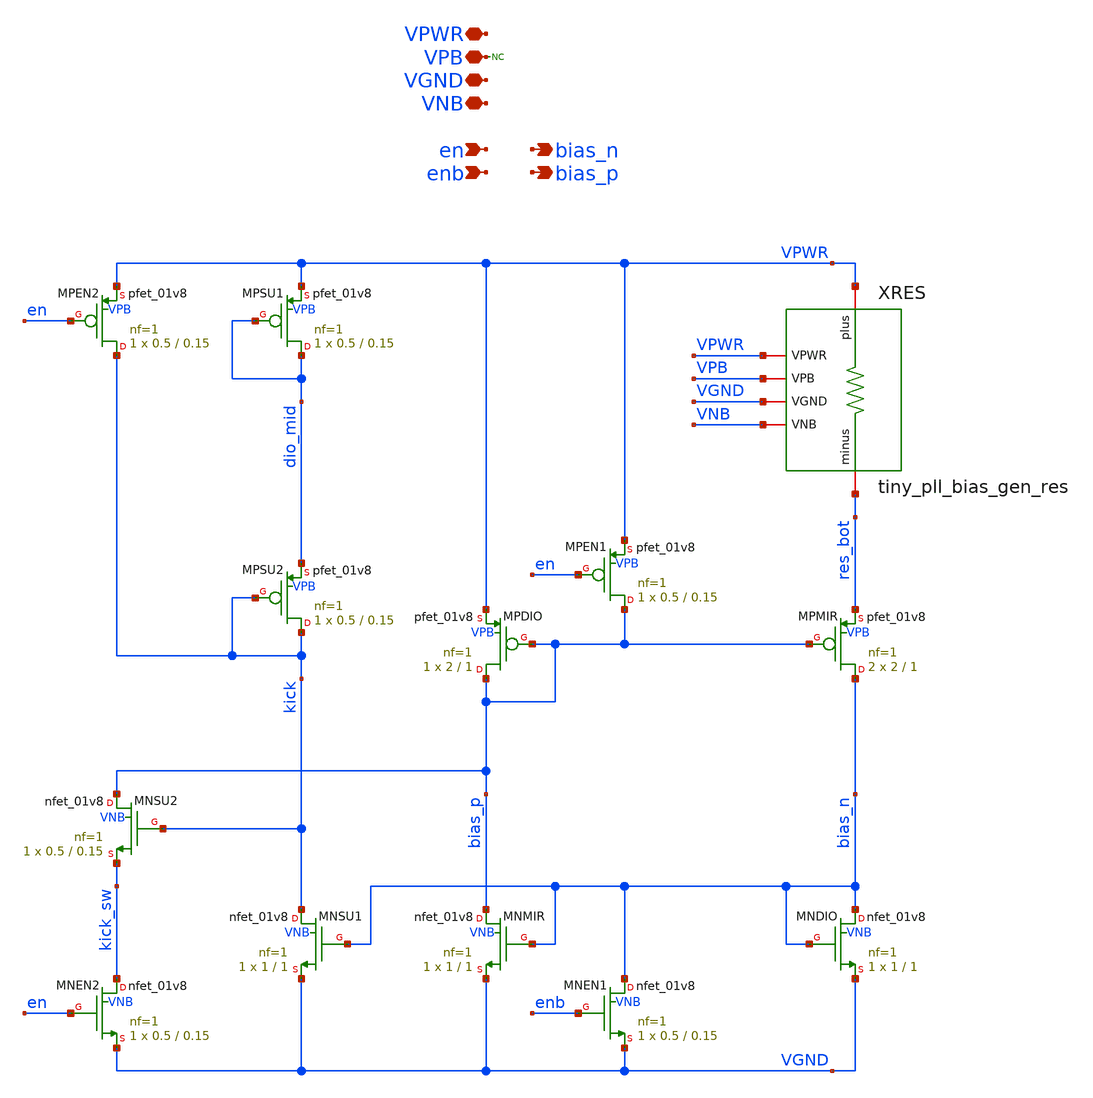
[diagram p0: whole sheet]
** sch_path: xschem/tiny_pll/tiny_pll_bias_gen.sch
**.subckt tiny_pll_bias_gen VNB VGND VPB VPWR bias_n enb en bias_p
*.iopin VNB
*.iopin VGND
*.iopin VPB
*.iopin VPWR
*.opin bias_n
*.ipin enb
*.ipin en
*.opin bias_p
XMNMIR bias_p bias_n VGND VNB sky130_fd_pr__nfet_01v8 L=1 W=1 nf=1 ad='int((nf+1)/2) * W/nf * 0.29' as='int((nf+2)/2) * W/nf * 0.29'
+ pd='2*int((nf+1)/2) * (W/nf + 0.29)' ps='2*int((nf+2)/2) * (W/nf + 0.29)' nrd='0.29 / W' nrs='0.29 / W'
+ sa=0 sb=0 sd=0 mult=1 m=1
XMNDIO bias_n bias_n VGND VNB sky130_fd_pr__nfet_01v8 L=1 W=1 nf=1 ad='int((nf+1)/2) * W/nf * 0.29' as='int((nf+2)/2) * W/nf * 0.29'
+ pd='2*int((nf+1)/2) * (W/nf + 0.29)' ps='2*int((nf+2)/2) * (W/nf + 0.29)' nrd='0.29 / W' nrs='0.29 / W'
+ sa=0 sb=0 sd=0 mult=1 m=1
XMPDIO bias_p bias_p VPWR VPB sky130_fd_pr__pfet_01v8 L=1 W=2 nf=1 ad='int((nf+1)/2) * W/nf * 0.29' as='int((nf+2)/2) * W/nf * 0.29'
+ pd='2*int((nf+1)/2) * (W/nf + 0.29)' ps='2*int((nf+2)/2) * (W/nf + 0.29)' nrd='0.29 / W' nrs='0.29 / W'
+ sa=0 sb=0 sd=0 mult=1 m=1
XMPMIR bias_n bias_p res_bot VPB sky130_fd_pr__pfet_01v8 L=1 W=2 nf=1 ad='int((nf+1)/2) * W/nf * 0.29'
+ as='int((nf+2)/2) * W/nf * 0.29' pd='2*int((nf+1)/2) * (W/nf + 0.29)' ps='2*int((nf+2)/2) * (W/nf + 0.29)'
+ nrd='0.29 / W' nrs='0.29 / W' sa=0 sb=0 sd=0 mult=2 m=2
* noconn VPB
XMNEN1 bias_n enb VGND VNB sky130_fd_pr__nfet_01v8 L=0.15 W=0.5 nf=1 ad='int((nf+1)/2) * W/nf * 0.29'
+ as='int((nf+2)/2) * W/nf * 0.29' pd='2*int((nf+1)/2) * (W/nf + 0.29)' ps='2*int((nf+2)/2) * (W/nf + 0.29)'
+ nrd='0.29 / W' nrs='0.29 / W' sa=0 sb=0 sd=0 mult=1 m=1
XMPEN1 bias_p en VPWR VPB sky130_fd_pr__pfet_01v8 L=0.15 W=0.5 nf=1 ad='int((nf+1)/2) * W/nf * 0.29'
+ as='int((nf+2)/2) * W/nf * 0.29' pd='2*int((nf+1)/2) * (W/nf + 0.29)' ps='2*int((nf+2)/2) * (W/nf + 0.29)'
+ nrd='0.29 / W' nrs='0.29 / W' sa=0 sb=0 sd=0 mult=1 m=1
XRES VGND VNB VPWR VPB VPWR res_bot tiny_pll_bias_gen_res
XMNSU1 kick bias_n VGND VNB sky130_fd_pr__nfet_01v8 L=1 W=1 nf=1 ad='int((nf+1)/2) * W/nf * 0.29' as='int((nf+2)/2) * W/nf * 0.29'
+ pd='2*int((nf+1)/2) * (W/nf + 0.29)' ps='2*int((nf+2)/2) * (W/nf + 0.29)' nrd='0.29 / W' nrs='0.29 / W'
+ sa=0 sb=0 sd=0 mult=1 m=1
XMNSU2 bias_p kick kick_sw VNB sky130_fd_pr__nfet_01v8 L=0.15 W=0.5 nf=1 ad='int((nf+1)/2) * W/nf * 0.29'
+ as='int((nf+2)/2) * W/nf * 0.29' pd='2*int((nf+1)/2) * (W/nf + 0.29)' ps='2*int((nf+2)/2) * (W/nf + 0.29)'
+ nrd='0.29 / W' nrs='0.29 / W' sa=0 sb=0 sd=0 mult=1 m=1
XMNEN2 kick_sw en VGND VNB sky130_fd_pr__nfet_01v8 L=0.15 W=0.5 nf=1 ad='int((nf+1)/2) * W/nf * 0.29'
+ as='int((nf+2)/2) * W/nf * 0.29' pd='2*int((nf+1)/2) * (W/nf + 0.29)' ps='2*int((nf+2)/2) * (W/nf + 0.29)'
+ nrd='0.29 / W' nrs='0.29 / W' sa=0 sb=0 sd=0 mult=1 m=1
XMPEN2 kick en VPWR VPB sky130_fd_pr__pfet_01v8 L=0.15 W=0.5 nf=1 ad='int((nf+1)/2) * W/nf * 0.29' as='int((nf+2)/2) * W/nf * 0.29'
+ pd='2*int((nf+1)/2) * (W/nf + 0.29)' ps='2*int((nf+2)/2) * (W/nf + 0.29)' nrd='0.29 / W' nrs='0.29 / W'
+ sa=0 sb=0 sd=0 mult=1 m=1
XMPSU2 kick kick dio_mid VPB sky130_fd_pr__pfet_01v8 L=0.15 W=0.5 nf=1 ad='int((nf+1)/2) * W/nf * 0.29'
+ as='int((nf+2)/2) * W/nf * 0.29' pd='2*int((nf+1)/2) * (W/nf + 0.29)' ps='2*int((nf+2)/2) * (W/nf + 0.29)'
+ nrd='0.29 / W' nrs='0.29 / W' sa=0 sb=0 sd=0 mult=1 m=1
XMPSU1 dio_mid dio_mid VPWR VPB sky130_fd_pr__pfet_01v8 L=0.15 W=0.5 nf=1 ad='int((nf+1)/2) * W/nf * 0.29'
+ as='int((nf+2)/2) * W/nf * 0.29' pd='2*int((nf+1)/2) * (W/nf + 0.29)' ps='2*int((nf+2)/2) * (W/nf + 0.29)'
+ nrd='0.29 / W' nrs='0.29 / W' sa=0 sb=0 sd=0 mult=1 m=1
**.ends

* expanding   symbol:  tiny_pll_bias_gen_res.sym # of pins=6
** sym_path: xschem/tiny_pll/tiny_pll_bias_gen_res.sym
** sch_path: xschem/tiny_pll/tiny_pll_bias_gen_res.sch
.subckt tiny_pll_bias_gen_res VGND VNB VPWR VPB plus minus
*.iopin minus
*.iopin plus
*.iopin VNB
*.iopin VGND
*.iopin VPB
*.iopin VPWR
XR2 mid1 plus VNB sky130_fd_pr__res_xhigh_po_0p35 L=1.8 mult=1 m=1
XR1 mid0 mid1 VNB sky130_fd_pr__res_xhigh_po_0p35 L=1.8 mult=1 m=1
XR0 minus mid0 VNB sky130_fd_pr__res_xhigh_po_0p35 L=1.8 mult=1 m=1
* noconn VPB
* noconn VPWR
* noconn VGND
.ends

.end
